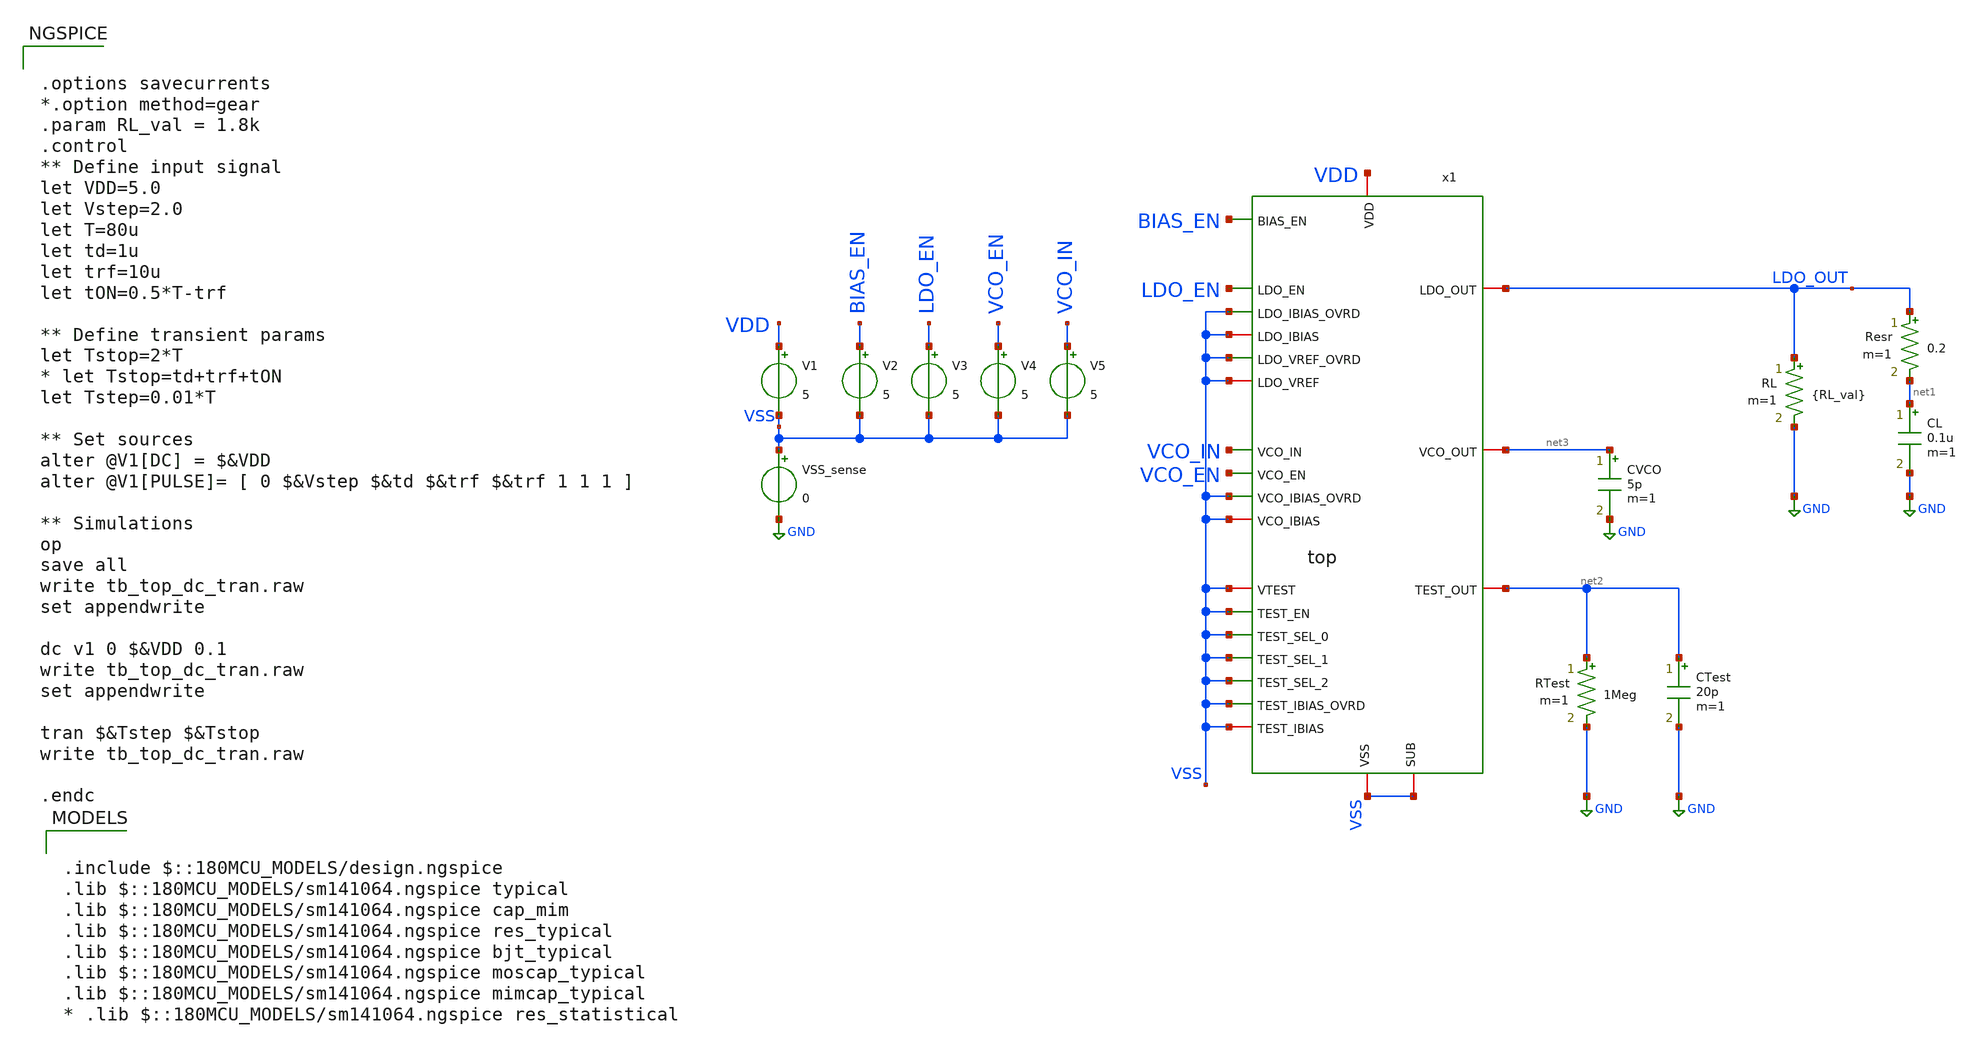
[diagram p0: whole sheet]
** sch_path: designs/libs/tb_top/tb_top_dc_tran/tb_top_dc_tran.sch
**.subckt tb_top_dc_tran
V1 VDD VSS 5
VSS_sense VSS GND 0
x1 VDD VCO_IN LDO_OUT net3 VCO_EN net2 VSS VSS VSS VSS VSS VSS VSS VSS LDO_EN VSS VSS VSS VSS VSS
+ VSS VSS BIAS_EN top
V2 BIAS_EN VSS 5
V3 LDO_EN VSS 5
V4 VCO_EN VSS 5
V5 VCO_IN VSS 5
RL LDO_OUT GND {RL_val} m=1
CL net1 GND 0.1u m=1
Resr LDO_OUT net1 0.2 m=1
RTest net2 GND 1Meg m=1
CTest net2 GND 20p m=1
CVCO net3 GND 5p m=1
**** begin user architecture code

.include $::180MCU_MODELS/design.ngspice
.lib $::180MCU_MODELS/sm141064.ngspice typical
.lib $::180MCU_MODELS/sm141064.ngspice cap_mim
.lib $::180MCU_MODELS/sm141064.ngspice res_typical
.lib $::180MCU_MODELS/sm141064.ngspice bjt_typical
.lib $::180MCU_MODELS/sm141064.ngspice moscap_typical
.lib $::180MCU_MODELS/sm141064.ngspice mimcap_typical
* .lib $::180MCU_MODELS/sm141064.ngspice res_statistical



.options savecurrents
*.option method=gear
.param RL_val = 1.8k
.control
** Define input signal
let VDD=5.0
let Vstep=2.0
let T=80u
let td=1u
let trf=10u
let tON=0.5*T-trf

** Define transient params
let Tstop=2*T
* let Tstop=td+trf+tON
let Tstep=0.01*T

** Set sources
alter @V1[DC] = $&VDD
alter @V1[PULSE]= [ 0 $&Vstep $&td $&trf $&trf 1 1 1 ]

** Simulations
op
save all
write tb_top_dc_tran.raw
set appendwrite

dc v1 0 $&VDD 0.1
write tb_top_dc_tran.raw
set appendwrite

tran $&Tstep $&Tstop
write tb_top_dc_tran.raw

.endc


**** end user architecture code
**.ends
.GLOBAL GND
.end
